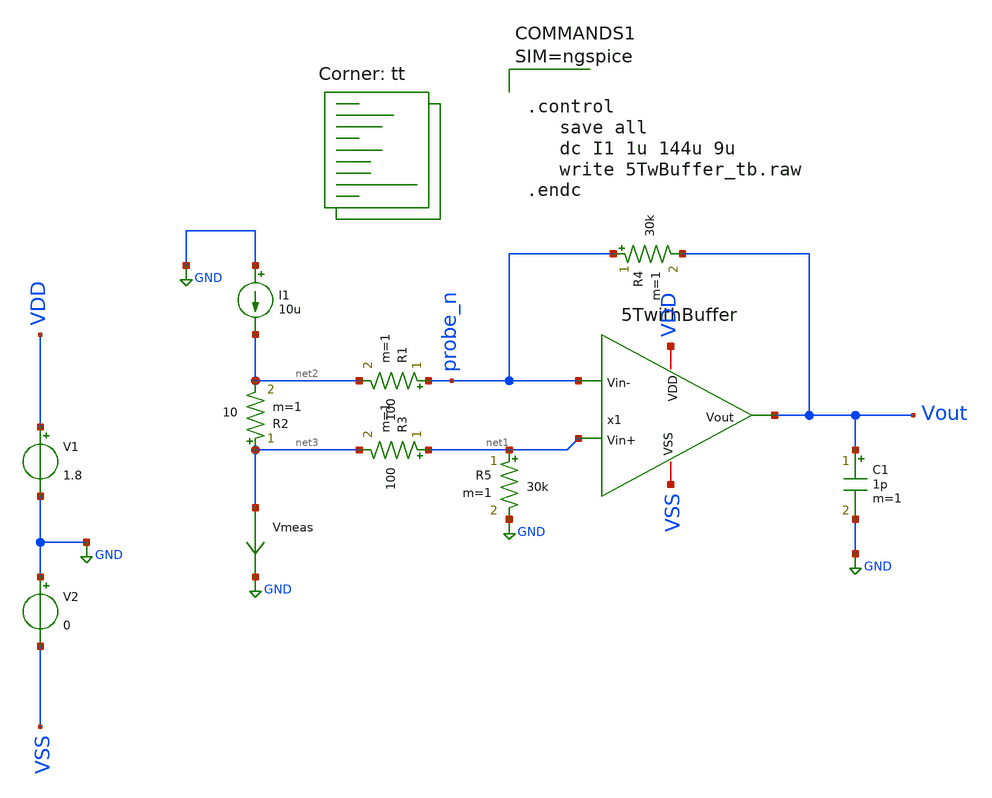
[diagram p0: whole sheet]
** sch_path: xschem/test/xschem/5TwBuffer_tb.sch
**.subckt 5TwBuffer_tb
x1 VDD Vout probe_n net1 VSS 5TwithBuffer
V1 VDD GND 1.8
V2 GND VSS 0
R2 net3 net2 10 m=1
C1 Vout GND 1p m=1
I1 GND net2 10u
Vmeas net3 GND 0
.save i(vmeas)
R4 probe_n Vout 30k m=1
R5 net1 GND 30k m=1
R1 probe_n net2 100 m=1
R3 net1 net3 100 m=1
**** begin user architecture code
.lib $::SKYWATER_MODELS/sky130.lib.spice tt



.control
   save all
   dc I1 1u 144u 9u
   write 5TwBuffer_tb.raw
.endc



**** end user architecture code
**.ends

* expanding   symbol:  amplifiers/dec24/5TwithBuffer.sym # of pins=5
** sym_path: amplifiers/dec24/5TwithBuffer.sym
** sch_path: amplifiers/dec24/5TwithBuffer.sch
.subckt 5TwithBuffer VDD Vout Vin- Vin+ VSS
*.iopin VDD
*.iopin VSS
*.ipin Vin-
*.ipin Vin+
*.opin Vout
I0 VDD Vb1 100u
XM1 net1 Vin+ Vsink VSS sky130_fd_pr__nfet_01v8 L=1 W=4 nf=1 ad='int((nf+1)/2) * W/nf * 0.29' as='int((nf+2)/2) * W/nf * 0.29'
+ pd='2*int((nf+1)/2) * (W/nf + 0.29)' ps='2*int((nf+2)/2) * (W/nf + 0.29)' nrd='0.29 / W' nrs='0.29 / W'
+ sa=0 sb=0 sd=0 mult=1 m=1
XM2 Vout Vin- Vsink VSS sky130_fd_pr__nfet_01v8 L=1 W=4 nf=1 ad='int((nf+1)/2) * W/nf * 0.29' as='int((nf+2)/2) * W/nf * 0.29'
+ pd='2*int((nf+1)/2) * (W/nf + 0.29)' ps='2*int((nf+2)/2) * (W/nf + 0.29)' nrd='0.29 / W' nrs='0.29 / W'
+ sa=0 sb=0 sd=0 mult=1 m=1
XM3 Vb1 Vb1 VSS VSS sky130_fd_pr__nfet_01v8 L=1 W=5 nf=1 ad='int((nf+1)/2) * W/nf * 0.29' as='int((nf+2)/2) * W/nf * 0.29'
+ pd='2*int((nf+1)/2) * (W/nf + 0.29)' ps='2*int((nf+2)/2) * (W/nf + 0.29)' nrd='0.29 / W' nrs='0.29 / W'
+ sa=0 sb=0 sd=0 mult=1 m=1
XM4 Vsink Vb1 VSS VSS sky130_fd_pr__nfet_01v8 L=1 W=5 nf=1 ad='int((nf+1)/2) * W/nf * 0.29' as='int((nf+2)/2) * W/nf * 0.29'
+ pd='2*int((nf+1)/2) * (W/nf + 0.29)' ps='2*int((nf+2)/2) * (W/nf + 0.29)' nrd='0.29 / W' nrs='0.29 / W'
+ sa=0 sb=0 sd=0 mult=1 m=1
XM7 VDD Vout net2 VSS sky130_fd_pr__nfet_01v8 L=1 W=20 nf=1 ad='int((nf+1)/2) * W/nf * 0.29' as='int((nf+2)/2) * W/nf * 0.29'
+ pd='2*int((nf+1)/2) * (W/nf + 0.29)' ps='2*int((nf+2)/2) * (W/nf + 0.29)' nrd='0.29 / W' nrs='0.29 / W'
+ sa=0 sb=0 sd=0 mult=1 m=1
XM8 net2 Vb1 VSS VSS sky130_fd_pr__nfet_01v8 L=1 W=5 nf=1 ad='int((nf+1)/2) * W/nf * 0.29' as='int((nf+2)/2) * W/nf * 0.29'
+ pd='2*int((nf+1)/2) * (W/nf + 0.29)' ps='2*int((nf+2)/2) * (W/nf + 0.29)' nrd='0.29 / W' nrs='0.29 / W'
+ sa=0 sb=0 sd=0 mult=5 m=5
XM5 net1 net1 VDD VDD sky130_fd_pr__pfet_01v8_lvt L=1 W=10 nf=1 ad='int((nf+1)/2) * W/nf * 0.29' as='int((nf+2)/2) * W/nf * 0.29'
+ pd='2*int((nf+1)/2) * (W/nf + 0.29)' ps='2*int((nf+2)/2) * (W/nf + 0.29)' nrd='0.29 / W' nrs='0.29 / W'
+ sa=0 sb=0 sd=0 mult=1 m=1
XM6 VDD net1 Vout VDD sky130_fd_pr__pfet_01v8_lvt L=1 W=10 nf=1 ad='int((nf+1)/2) * W/nf * 0.29' as='int((nf+2)/2) * W/nf * 0.29'
+ pd='2*int((nf+1)/2) * (W/nf + 0.29)' ps='2*int((nf+2)/2) * (W/nf + 0.29)' nrd='0.29 / W' nrs='0.29 / W'
+ sa=0 sb=0 sd=0 mult=1 m=1
.ends

.GLOBAL GND
.GLOBAL VDD
.end
